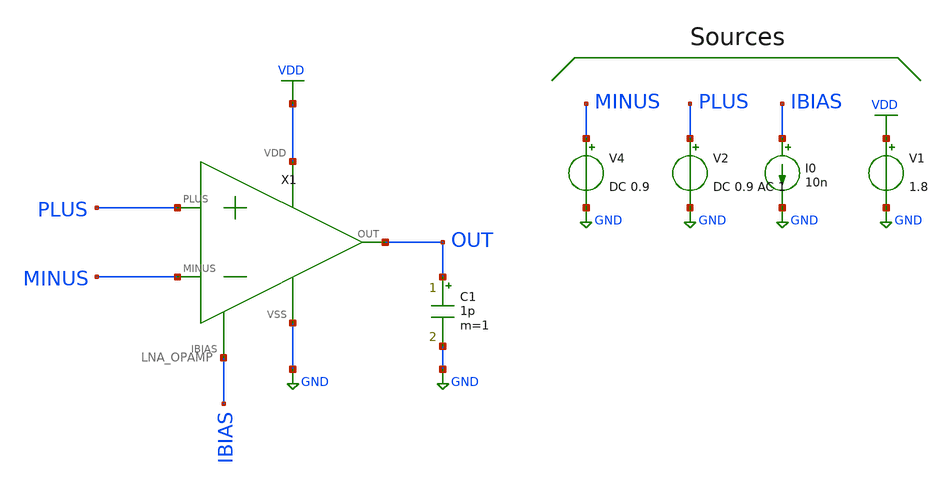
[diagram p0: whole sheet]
** sch_path: xschem/LNA/LNA_OPAMP_TB_OL.sch
**.subckt LNA_OPAMP_TB_OL
I0 IBIAS GND 10n
V1 VDD GND 1.8
V2 PLUS GND DC 0.9 AC 1
V4 MINUS GND DC 0.9
C1 OUT GND 1p m=1
X1 PLUS MINUS OUT IBIAS GND VDD LNA_OPAMP
**** begin user architecture code



*.include ~/OpenPDK/skywater-pdk/skywater-pdk/libraries/sky130_fd_pr/latest/cells/pfet_g5v0d10v5/sky130_fd_pr__pfet_g5v0d10v5__tt.corner.spice
*.include ~/OpenPDK/skywater-pdk/skywater-pdk/libraries/sky130_fd_pr/latest/cells/pfet_g5v0d10v5/sky130_fd_pr__pfet_g5v0d10v5__mismatch.corner.spice
*.include ~/OpenPDK/skywater-pdk/skywater-pdk/libraries/sky130_fd_pr/latest/cells/pfet_g5v0d10v5/sky130_fd_pr__nfet_g5v0d10v5__tt.corner.spice
*.include ~/OpenPDK/skywater-pdk/skywater-pdk/libraries/sky130_fd_pr/latest/cells/pfet_g5v0d10v5/sky130_fd_pr__nfet_g5v0d10v5__mismatch.corner.spice

.include /usr/share/pdk/sky130A/libs.ref/spi/sky130_fd_pr/sky130_fd_pr__nfet_01v8_lvt__tt.corner.spice
.include /usr/share/pdk/sky130A/libs.ref/spi/sky130_fd_pr/sky130_fd_pr__nfet_01v8_lvt__mismatch.corner.spice
.include /usr/share/pdk/sky130A/libs.ref/spi/sky130_fd_pr/sky130_fd_pr__pfet_01v8_lvt__tt.corner.spice
.include /usr/share/pdk/sky130A/libs.ref/spi/sky130_fd_pr/sky130_fd_pr__pfet_01v8_lvt__mismatch.corner.spice

.include ~/OpenPDK/skywater-pdk/skywater-pdk/libraries/sky130_fd_pr/latest/models/all.spice





.option gmin=1E-14

.control

op
*dc V2 0.85 0.95 10u
*plot OUT
*plot deriv(OUT)

ac dec 100 1 10MEG
plot db(OUT)

*set sqrnoise
noise v(out) V2 dec 100 50m 100
*setplot noise1
*plot log(inoise_spectrum)
*plot onoise_spectrum

print inoise_total
*print onoise_total

.endc


**** end user architecture code
**.ends
.GLOBAL VDD
.GLOBAL GND
.end
